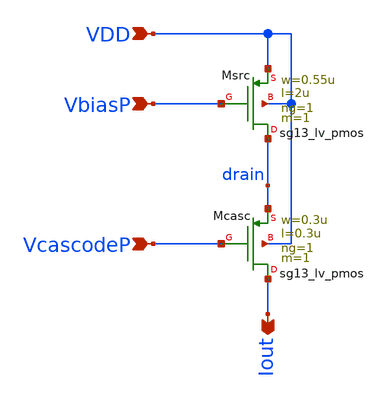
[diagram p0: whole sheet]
** sch_path: xschem/pcsource.sch
**.subckt pcsource VcascodeP VbiasP Iout VDD
*.ipin VcascodeP
*.ipin VbiasP
*.opin Iout
*.ipin VDD
XMsrc drain VbiasP VDD VDD sg13_lv_pmos w=0.55u l=2u ng=1 m=1 mm_ok=1
XMcasc Iout VcascodeP drain VDD sg13_lv_pmos w=0.3u l=0.3u ng=1 m=1 mm_ok=1
**.ends
.end
